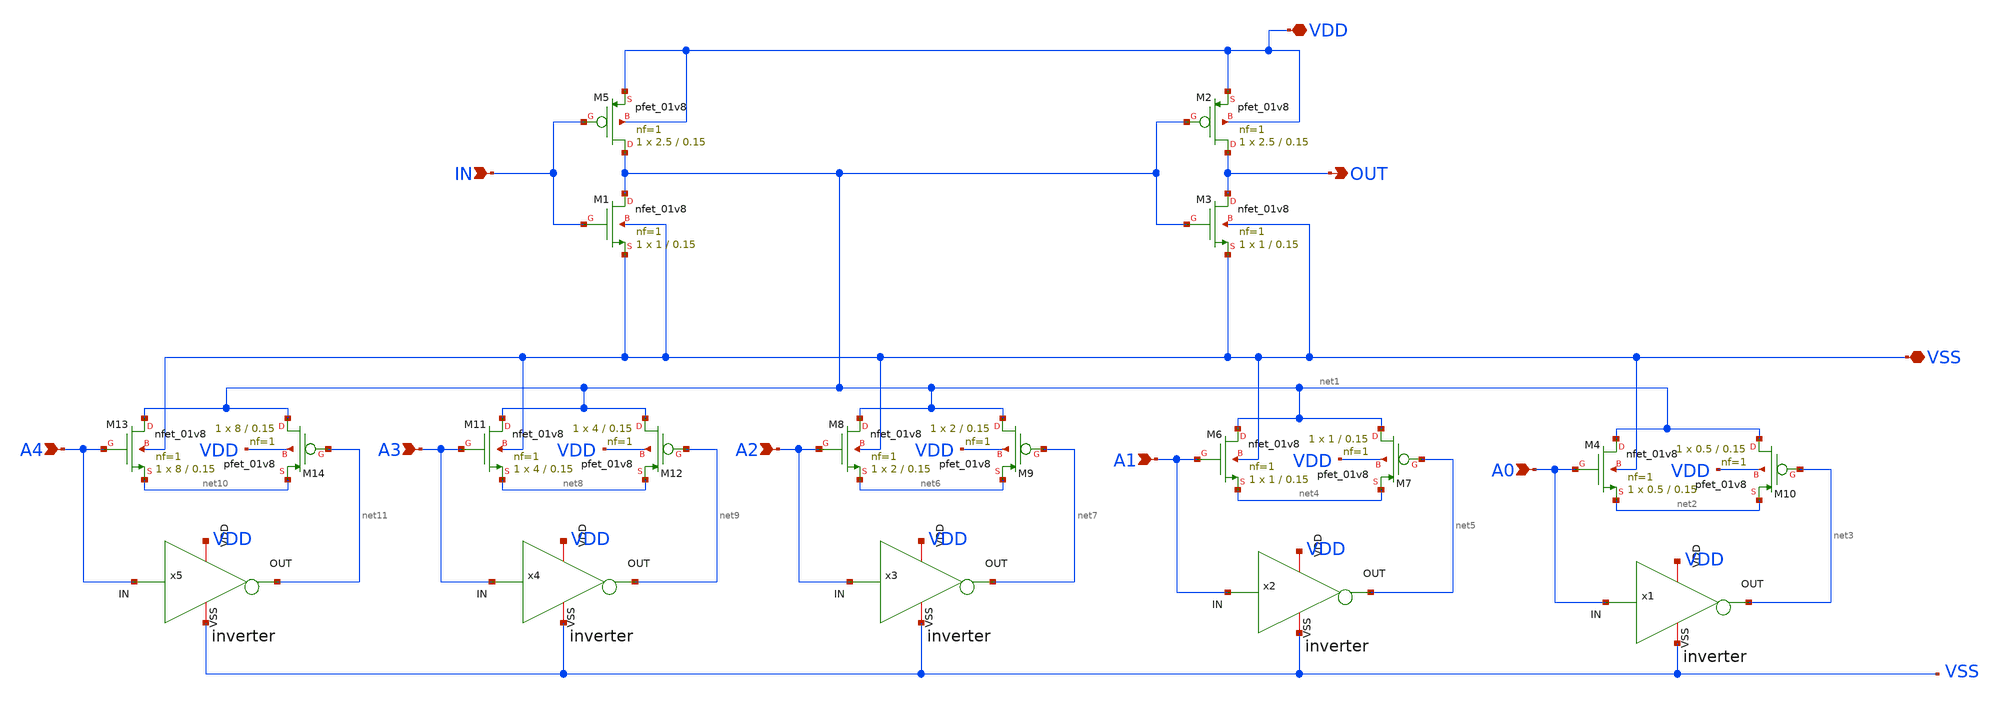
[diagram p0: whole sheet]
** sch_path: xschem/schematic/SCI_DCDL/TG_SCI/SCI_TG_5bit.sch
**.subckt SCI_TG_5bit IN OUT VDD VSS A0 A1 A2 A3 A4
*.ipin IN
*.opin OUT
*.iopin VDD
*.iopin VSS
*.ipin A0
*.ipin A1
*.ipin A2
*.ipin A3
*.ipin A4
XM1 net1 IN VSS VSS sky130_fd_pr__nfet_01v8 L=0.15 W=1 nf=1 ad='int((1 + 1)/2) * 1 / 1 * 0.29' as='int((1 + 2)/2) * 1 / 1 * 0.29'
+ pd='2*int((1 + 1)/2) * (1 / 1 + 0.29)' ps='2*int((1 + 2)/2) * (1 / 1 + 0.29)' nrd='0.29 / 1 ' nrs='0.29 / 1 '
+ sa=0 sb=0 sd=0 mult=1 m=1
XM3 OUT net1 VSS VSS sky130_fd_pr__nfet_01v8 L=0.15 W=1 nf=1 ad='int((1 + 1)/2) * 1 / 1 * 0.29' as='int((1 + 2)/2) * 1 / 1 * 0.29'
+ pd='2*int((1 + 1)/2) * (1 / 1 + 0.29)' ps='2*int((1 + 2)/2) * (1 / 1 + 0.29)' nrd='0.29 / 1 ' nrs='0.29 / 1 '
+ sa=0 sb=0 sd=0 mult=1 m=1
XM5 net1 IN VDD VDD sky130_fd_pr__pfet_01v8 L=0.15 W=2.5 nf=1 ad='int((1 + 1)/2) * 2.5 / 1 * 0.29' as='int((1 + 2)/2) * 2.5 / 1 * 0.29'
+ pd='2*int((1 + 1)/2) * (2.5 / 1 + 0.29)' ps='2*int((1 + 2)/2) * (2.5 / 1 + 0.29)' nrd='0.29 / 2.5 ' nrs='0.29 / 2.5 '
+ sa=0 sb=0 sd=0 mult=1 m=1
XM2 OUT net1 VDD VDD sky130_fd_pr__pfet_01v8 L=0.15 W=2.5 nf=1 ad='int((1 + 1)/2) * 2.5 / 1 * 0.29' as='int((1 + 2)/2) * 2.5 / 1 * 0.29'
+ pd='2*int((1 + 1)/2) * (2.5 / 1 + 0.29)' ps='2*int((1 + 2)/2) * (2.5 / 1 + 0.29)' nrd='0.29 / 2.5 ' nrs='0.29 / 2.5 '
+ sa=0 sb=0 sd=0 mult=1 m=1
XM4 net1 A0 net2 VSS sky130_fd_pr__nfet_01v8 L=0.15 W=0.5 nf=1 ad='int((1 + 1)/2) * 0.5 / 1 * 0.29' as='int((1 + 2)/2) * 0.5 / 1 * 0.29'
+ pd='2*int((1 + 1)/2) * (0.5 / 1 + 0.29)' ps='2*int((1 + 2)/2) * (0.5 / 1 + 0.29)' nrd='0.29 / 0.5 ' nrs='0.29 / 0.5 '
+ sa=0 sb=0 sd=0 mult=1 m=1
XM10 net1 net3 net2 VDD sky130_fd_pr__pfet_01v8 L=0.15 W=0.5 nf=1 ad='int((1 + 1)/2) * 0.5 / 1 * 0.29'
+ as='int((1 + 2)/2) * 0.5 / 1 * 0.29' pd='2*int((1 + 1)/2) * (0.5 / 1 + 0.29)' ps='2*int((1 + 2)/2) * (0.5 / 1 + 0.29)'
+ nrd='0.29 / 0.5 ' nrs='0.29 / 0.5 ' sa=0 sb=0 sd=0 mult=1 m=1
x1 VDD A0 net3 VSS inverter
XM6 net1 A1 net4 VSS sky130_fd_pr__nfet_01v8 L=0.15 W=1 nf=1 ad='int((1 + 1)/2) * 1 / 1 * 0.29' as='int((1 + 2)/2) * 1 / 1 * 0.29'
+ pd='2*int((1 + 1)/2) * (1 / 1 + 0.29)' ps='2*int((1 + 2)/2) * (1 / 1 + 0.29)' nrd='0.29 / 1 ' nrs='0.29 / 1 '
+ sa=0 sb=0 sd=0 mult=1 m=1
XM7 net1 net5 net4 VDD sky130_fd_pr__pfet_01v8 L=0.15 W=1 nf=1 ad='int((1 + 1)/2) * 1 / 1 * 0.29' as='int((1 + 2)/2) * 1 / 1 * 0.29'
+ pd='2*int((1 + 1)/2) * (1 / 1 + 0.29)' ps='2*int((1 + 2)/2) * (1 / 1 + 0.29)' nrd='0.29 / 1 ' nrs='0.29 / 1 '
+ sa=0 sb=0 sd=0 mult=1 m=1
x2 VDD A1 net5 VSS inverter
XM8 net1 A2 net6 VSS sky130_fd_pr__nfet_01v8 L=0.15 W=2 nf=1 ad='int((1 + 1)/2) * 2 / 1 * 0.29' as='int((1 + 2)/2) * 2 / 1 * 0.29'
+ pd='2*int((1 + 1)/2) * (2 / 1 + 0.29)' ps='2*int((1 + 2)/2) * (2 / 1 + 0.29)' nrd='0.29 / 2 ' nrs='0.29 / 2 '
+ sa=0 sb=0 sd=0 mult=1 m=1
XM9 net1 net7 net6 VDD sky130_fd_pr__pfet_01v8 L=0.15 W=2 nf=1 ad='int((1 + 1)/2) * 2 / 1 * 0.29' as='int((1 + 2)/2) * 2 / 1 * 0.29'
+ pd='2*int((1 + 1)/2) * (2 / 1 + 0.29)' ps='2*int((1 + 2)/2) * (2 / 1 + 0.29)' nrd='0.29 / 2 ' nrs='0.29 / 2 '
+ sa=0 sb=0 sd=0 mult=1 m=1
x3 VDD A2 net7 VSS inverter
XM11 net1 A3 net8 VSS sky130_fd_pr__nfet_01v8 L=0.15 W=4 nf=1 ad='int((1 + 1)/2) * 4 / 1 * 0.29' as='int((1 + 2)/2) * 4 / 1 * 0.29'
+ pd='2*int((1 + 1)/2) * (4 / 1 + 0.29)' ps='2*int((1 + 2)/2) * (4 / 1 + 0.29)' nrd='0.29 / 4 ' nrs='0.29 / 4 '
+ sa=0 sb=0 sd=0 mult=1 m=1
XM12 net1 net9 net8 VDD sky130_fd_pr__pfet_01v8 L=0.15 W=4 nf=1 ad='int((1 + 1)/2) * 4 / 1 * 0.29' as='int((1 + 2)/2) * 4 / 1 * 0.29'
+ pd='2*int((1 + 1)/2) * (4 / 1 + 0.29)' ps='2*int((1 + 2)/2) * (4 / 1 + 0.29)' nrd='0.29 / 4 ' nrs='0.29 / 4 '
+ sa=0 sb=0 sd=0 mult=1 m=1
x4 VDD A3 net9 VSS inverter
XM13 net1 A4 net10 VSS sky130_fd_pr__nfet_01v8 L=0.15 W=8 nf=1 ad='int((1 + 1)/2) * 8 / 1 * 0.29' as='int((1 + 2)/2) * 8 / 1 * 0.29'
+ pd='2*int((1 + 1)/2) * (8 / 1 + 0.29)' ps='2*int((1 + 2)/2) * (8 / 1 + 0.29)' nrd='0.29 / 8 ' nrs='0.29 / 8 '
+ sa=0 sb=0 sd=0 mult=1 m=1
XM14 net1 net11 net10 VDD sky130_fd_pr__pfet_01v8 L=0.15 W=8 nf=1 ad='int((1 + 1)/2) * 8 / 1 * 0.29'
+ as='int((1 + 2)/2) * 8 / 1 * 0.29' pd='2*int((1 + 1)/2) * (8 / 1 + 0.29)' ps='2*int((1 + 2)/2) * (8 / 1 + 0.29)'
+ nrd='0.29 / 8 ' nrs='0.29 / 8 ' sa=0 sb=0 sd=0 mult=1 m=1
x5 VDD A4 net11 VSS inverter
**.ends

* expanding   symbol:  inverter.sym # of pins=4
** sym_path: xschem/schematic/SCI_DCDL/TG_SCI/inverter.sym
** sch_path: xschem/schematic/SCI_DCDL/TG_SCI/inverter.sch
.subckt inverter VDD IN OUT VSS
*.ipin IN
*.opin OUT
*.iopin VDD
*.iopin VSS
XM1 OUT IN VSS VSS sky130_fd_pr__nfet_01v8 L=0.15 W=1 nf=1 ad='int((1 + 1)/2) * 1 / 1 * 0.29' as='int((1 + 2)/2) * 1 / 1 * 0.29'
+ pd='2*int((1 + 1)/2) * (1 / 1 + 0.29)' ps='2*int((1 + 2)/2) * (1 / 1 + 0.29)' nrd='0.29 / 1 ' nrs='0.29 / 1 '
+ sa=0 sb=0 sd=0 mult=1 m=1
XM2 OUT IN VDD VDD sky130_fd_pr__pfet_01v8 L=0.15 W=1 nf=1 ad='int((1 + 1)/2) * 1 / 1 * 0.29' as='int((1 + 2)/2) * 1 / 1 * 0.29'
+ pd='2*int((1 + 1)/2) * (1 / 1 + 0.29)' ps='2*int((1 + 2)/2) * (1 / 1 + 0.29)' nrd='0.29 / 1 ' nrs='0.29 / 1 '
+ sa=0 sb=0 sd=0 mult=1 m=1
.ends

.end
